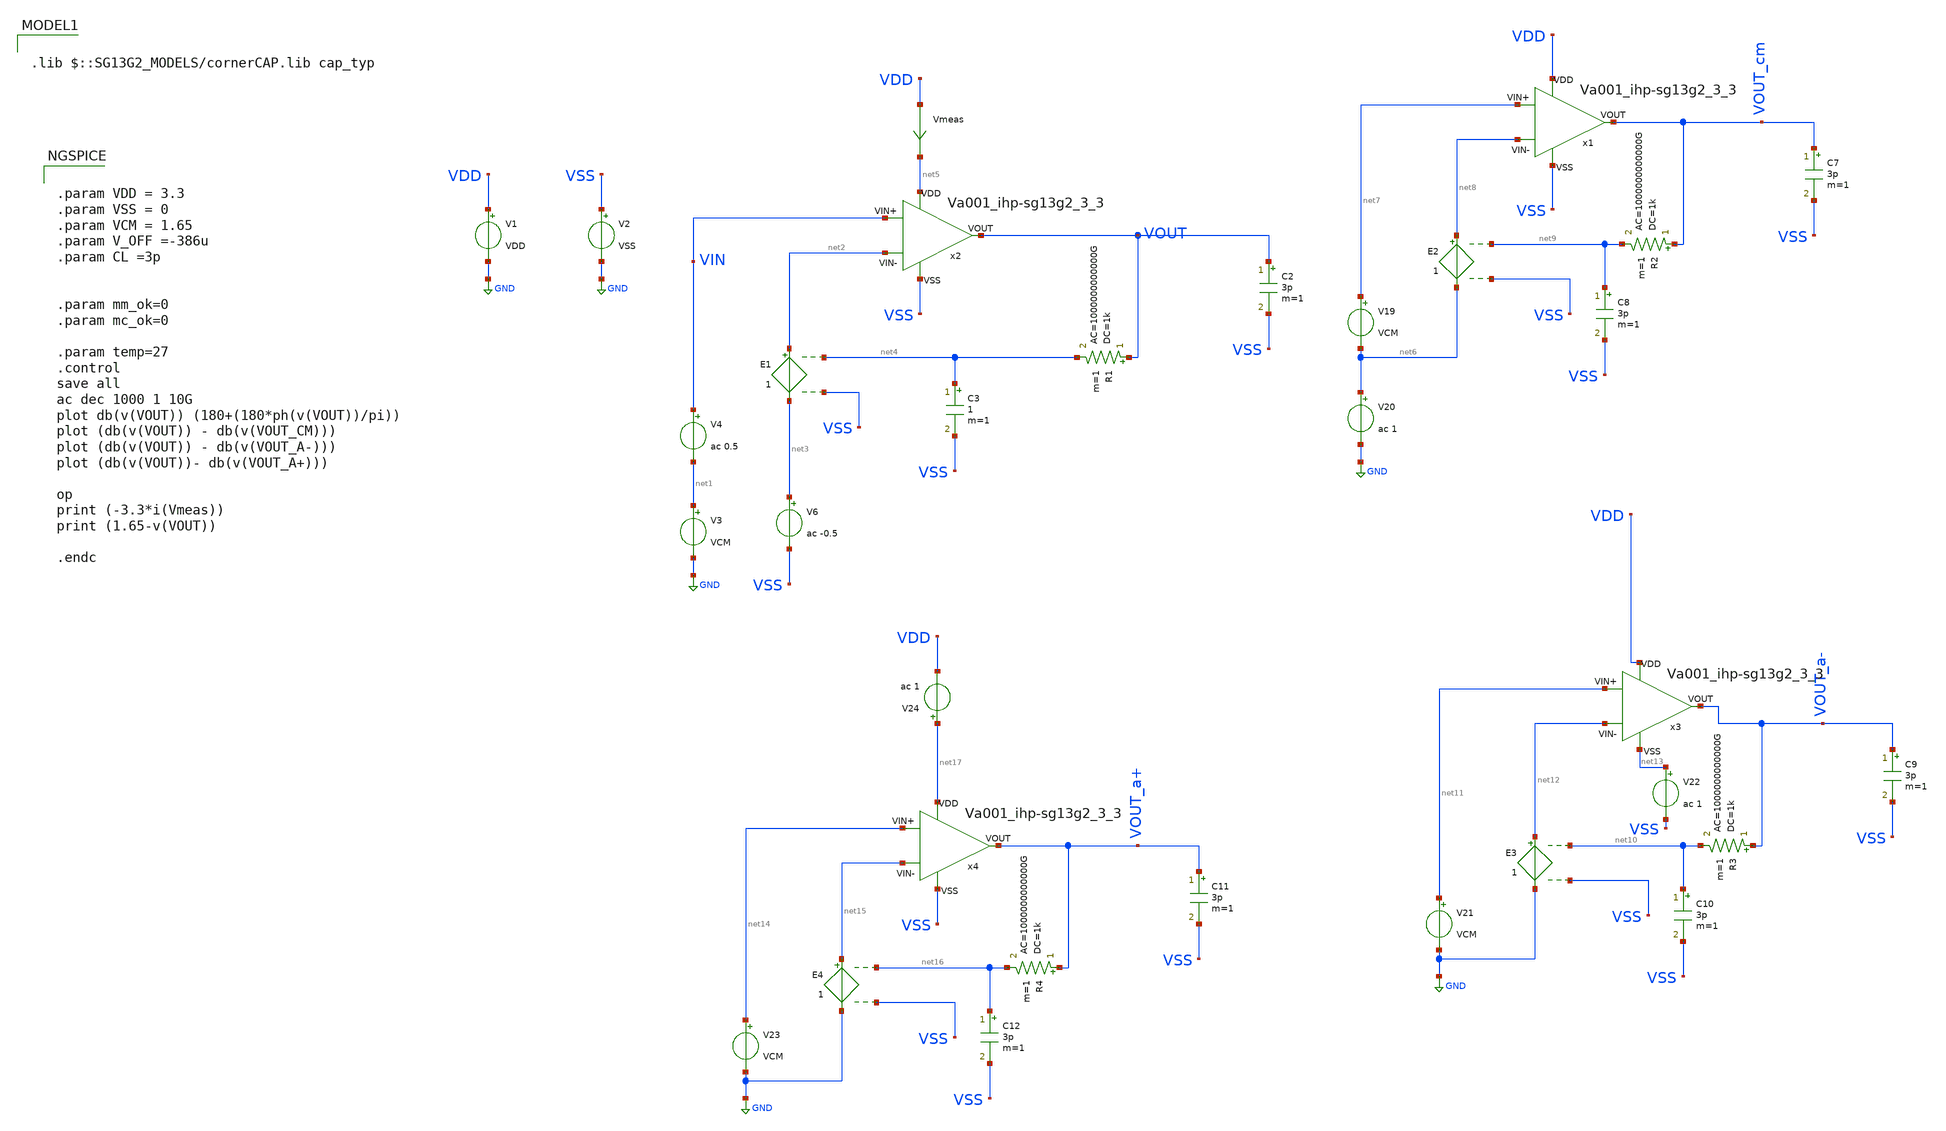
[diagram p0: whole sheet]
** sch_path: Learning/single_ended_amplifiers/VA001_series/Design_and_Analysis_of_Two-Stage_CMOS_Operational_Amplifier_for_Fluorescence_Signal_Processing_ihp130_3_3V/amplifier_design/full_sim.sch
**.subckt full_sim
V1 VDD GND VDD
V2 VSS GND VSS
V3 net1 GND VCM
V4 VIN net1 ac 0.5
V6 net3 VSS ac -0.5
E1 net2 net3 net4 VSS 1
C2 VOUT VSS 3p m=1
R1 VOUT net4 1k ac=1000000000000G m=1
C3 net4 VSS 1 m=1
x2 net5 VSS net2 VIN VOUT Va001_ihp-sg13g2_3_3
C7 VOUT_cm VSS 3p m=1
V19 net7 net6 VCM
V20 net6 GND ac 1
E2 net8 net6 net9 VSS 1
R2 VOUT_cm net9 1k ac=1000000000000G m=1
C8 net9 VSS 3p m=1
x1 VDD VSS net8 net7 VOUT_cm Va001_ihp-sg13g2_3_3
Vmeas VDD net5 0
.save i(vmeas)
C9 VOUT_a- VSS 3p m=1
V21 net11 GND VCM
E3 net12 GND net10 VSS 1
R3 VOUT_a- net10 1k ac=1000000000000G m=1
C10 net10 VSS 3p m=1
V22 net13 VSS ac 1
x3 VDD net13 net12 net11 VOUT_a- Va001_ihp-sg13g2_3_3
C11 VOUT_a+ VSS 3p m=1
V23 net14 GND VCM
E4 net15 GND net16 VSS 1
R4 VOUT_a+ net16 1k ac=1000000000000G m=1
C12 net16 VSS 3p m=1
V24 net17 VDD ac 1
x4 net17 VSS net15 net14 VOUT_a+ Va001_ihp-sg13g2_3_3
**** begin user architecture code

.lib $::SG13G2_MODELS/cornerRES.lib res_typ


.lib cornerMOShv.lib mos_tt


.lib $::SG13G2_MODELS/cornerCAP.lib cap_typ

**** end user architecture code
**.ends

* expanding   symbol:  ihp-sg13g2/Amplifiers/Va001_ihp-sg13g2_3_3.sym # of pins=5
** sym_path: LIB/ihp-sg13g2/Amplifiers/Va001_ihp-sg13g2_3_3.sym
** sch_path: LIB/ihp-sg13g2/Amplifiers/Va001_ihp-sg13g2_3_3.sch
.subckt Va001_ihp-sg13g2_3_3 VDD VSS VIN- VIN+ VOUT
*.iopin VDD
*.iopin VSS
*.iopin VIN-
*.iopin VIN+
*.iopin VOUT
XM2 VB1 VB1 VDD VDD sg13_hv_pmos w=1.5u l=2u ng=2 m=2 mm_ok=1
XM1 VB2 VB1 VDD VDD sg13_hv_pmos w=1.5u l=2u ng=2 m=2 mm_ok=1
XM3 VB1 VB2 net3 VSS sg13_hv_nmos w=1.0u l=2u ng=2 m=2 mm_ok=1
XM4 VB2 VB2 net1 VSS sg13_hv_nmos w=1.0u l=2u ng=2 m=2 mm_ok=1
XM5 net3 net1 net2 VSS sg13_hv_nmos w=2u l=2u ng=2 m=8 mm_ok=1
XM6 net1 net1 VSS VSS sg13_hv_nmos w=2u l=2u ng=2 m=2 mm_ok=1
XR1 net2 VSS sub! rhigh w=0.5e-6 l=5.9e-6 m=1 b=0 mm_ok=1
XM7 net4 VB1 VDD VDD sg13_hv_pmos w=1.5u l=2u ng=2 m=8 mm_ok=1
XM9 net6 VIN+ net4 net4 sg13_hv_pmos w=8u l=0.8u ng=4 m=4 mm_ok=1
XM8 net5 VIN- net4 net4 sg13_hv_pmos w=8u l=0.8u ng=4 m=4 mm_ok=1
XM10 net5 net5 VSS VSS sg13_hv_nmos w=2u l=2u ng=2 m=2 mm_ok=1
XM11 net6 net5 VSS VSS sg13_hv_nmos w=2u l=2u ng=2 m=2 mm_ok=1
XM12 VOUT VB1 VDD VDD sg13_hv_pmos w=1.5u l=2u ng=2 m=16 mm_ok=1
XM13 VOUT net6 VSS VSS sg13_hv_nmos w=2u l=0.8u ng=2 m=4 mm_ok=1
XM14 net6 VB2 net7 VSS sg13_hv_nmos w=2u l=2.7u ng=1 m=2 mm_ok=1
XC1 VOUT net7 cap_cmim w=9e-6 l=9e-6 m=4 mm_ok=1
.ends

.GLOBAL GND
**** begin user architecture code


.param VDD = 3.3
.param VSS = 0
.param VCM = 1.65
.param V_OFF =-386u
.param CL =3p


.param mm_ok=0
.param mc_ok=0

.param temp=27
.control
save all
ac dec 1000 1 10G
plot db(v(VOUT)) (180+(180*ph(v(VOUT))/pi))
plot (db(v(VOUT)) - db(v(VOUT_CM)))
plot (db(v(VOUT)) - db(v(VOUT_A-)))
plot (db(v(VOUT))- db(v(VOUT_A+)))

op
print (-3.3*i(Vmeas))
print (1.65-v(VOUT))

.endc


**** end user architecture code
.end
